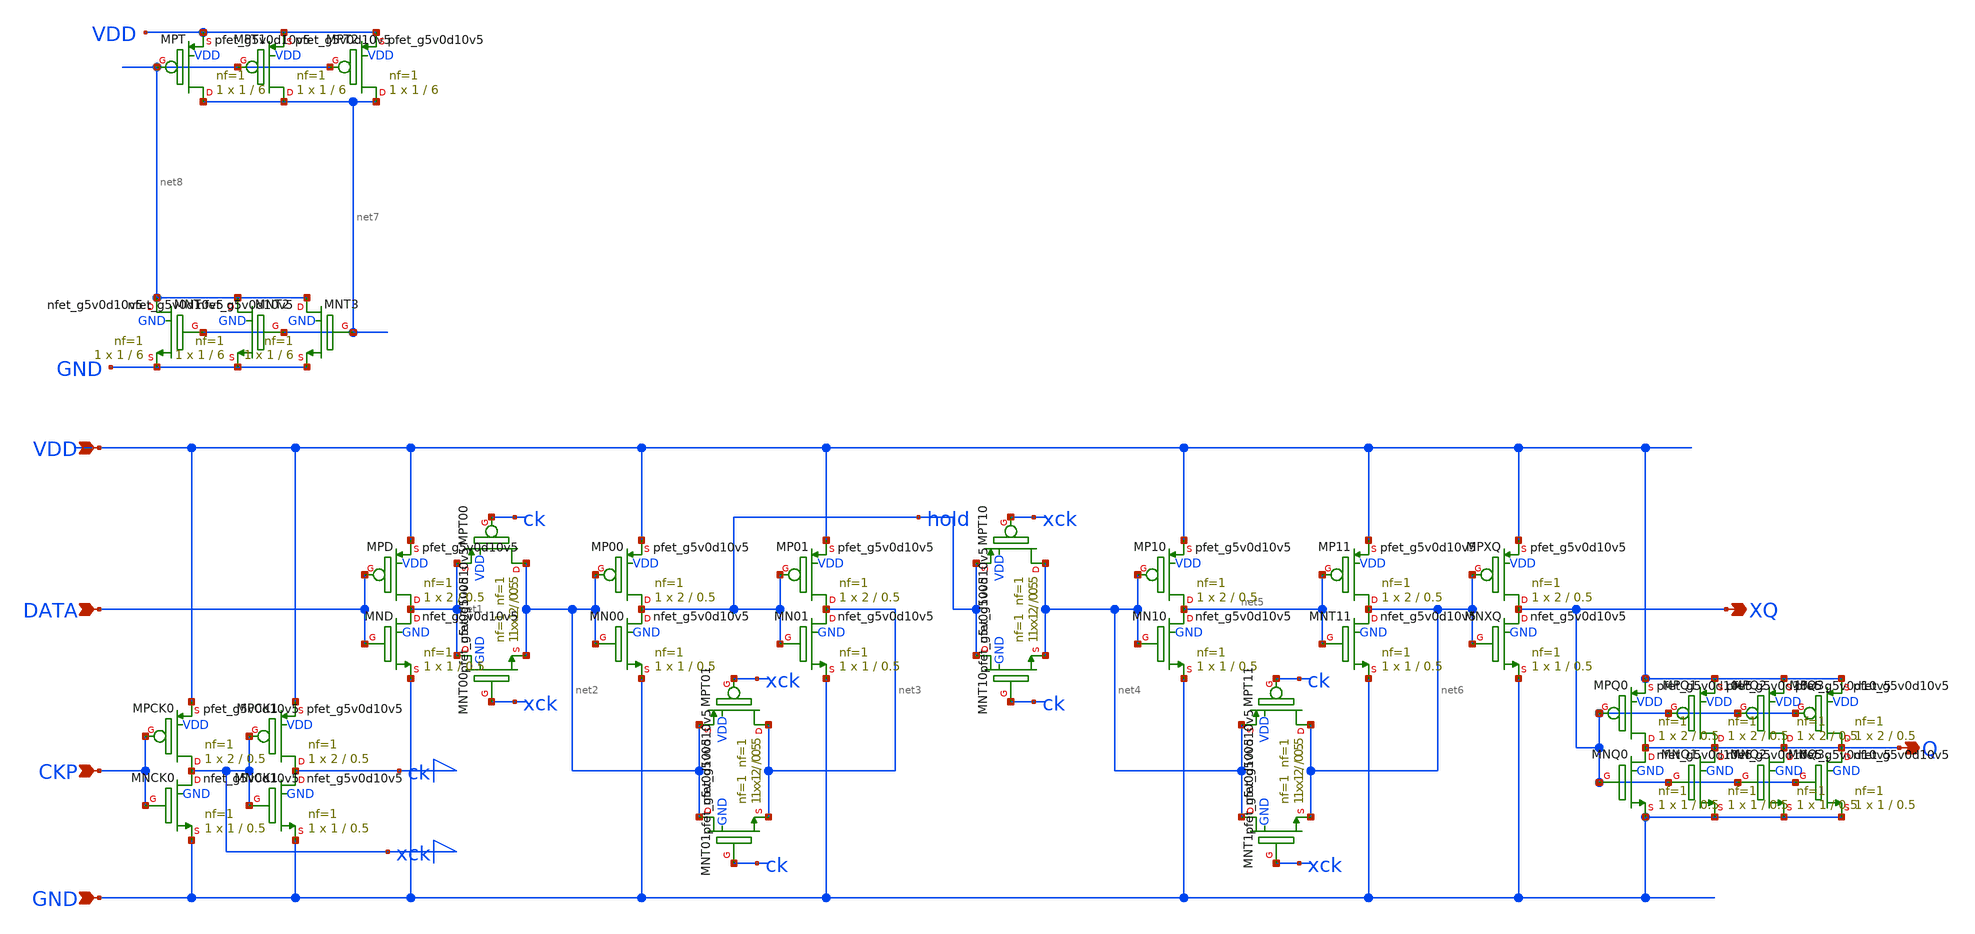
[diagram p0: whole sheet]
** sch_path: design/schematic/DFF3V3_v1.sch
**.subckt DFF3V3_v1 VDD DATA GND CKP XQ Q
*.ipin VDD
*.ipin DATA
*.ipin GND
*.ipin CKP
*.opin XQ
*.opin Q
XMNCK0 xck CKP GND GND sky130_fd_pr__nfet_g5v0d10v5 L=0.5 W=1 nf=1 ad='int((nf+1)/2) * W/nf * 0.29' as='int((nf+2)/2) * W/nf * 0.29'
+ pd='2*int((nf+1)/2) * (W/nf + 0.29)' ps='2*int((nf+2)/2) * (W/nf + 0.29)' nrd='0.29 / W' nrs='0.29 / W'
+ sa=0 sb=0 sd=0 mult=1 m=1
XMPCK0 xck CKP VDD VDD sky130_fd_pr__pfet_g5v0d10v5 L=0.5 W=2 nf=1 ad='int((nf+1)/2) * W/nf * 0.29' as='int((nf+2)/2) * W/nf * 0.29'
+ pd='2*int((nf+1)/2) * (W/nf + 0.29)' ps='2*int((nf+2)/2) * (W/nf + 0.29)' nrd='0.29 / W' nrs='0.29 / W'
+ sa=0 sb=0 sd=0 mult=1 m=1
XMNCK1 ck xck GND GND sky130_fd_pr__nfet_g5v0d10v5 L=0.5 W=1 nf=1 ad='int((nf+1)/2) * W/nf * 0.29' as='int((nf+2)/2) * W/nf * 0.29'
+ pd='2*int((nf+1)/2) * (W/nf + 0.29)' ps='2*int((nf+2)/2) * (W/nf + 0.29)' nrd='0.29 / W' nrs='0.29 / W'
+ sa=0 sb=0 sd=0 mult=1 m=1
XMPCK1 ck xck VDD VDD sky130_fd_pr__pfet_g5v0d10v5 L=0.5 W=2 nf=1 ad='int((nf+1)/2) * W/nf * 0.29' as='int((nf+2)/2) * W/nf * 0.29'
+ pd='2*int((nf+1)/2) * (W/nf + 0.29)' ps='2*int((nf+2)/2) * (W/nf + 0.29)' nrd='0.29 / W' nrs='0.29 / W'
+ sa=0 sb=0 sd=0 mult=1 m=1
XMPT00 net2 ck net1 VDD sky130_fd_pr__pfet_g5v0d10v5 L=0.5 W=2 nf=1 ad='int((nf+1)/2) * W/nf * 0.29'
+ as='int((nf+2)/2) * W/nf * 0.29' pd='2*int((nf+1)/2) * (W/nf + 0.29)' ps='2*int((nf+2)/2) * (W/nf + 0.29)'
+ nrd='0.29 / W' nrs='0.29 / W' sa=0 sb=0 sd=0 mult=1 m=1
XMNT00 net1 xck net2 GND sky130_fd_pr__nfet_g5v0d10v5 L=0.5 W=1 nf=1 ad='int((nf+1)/2) * W/nf * 0.29'
+ as='int((nf+2)/2) * W/nf * 0.29' pd='2*int((nf+1)/2) * (W/nf + 0.29)' ps='2*int((nf+2)/2) * (W/nf + 0.29)'
+ nrd='0.29 / W' nrs='0.29 / W' sa=0 sb=0 sd=0 mult=1 m=1
XMN00 hold net2 GND GND sky130_fd_pr__nfet_g5v0d10v5 L=0.5 W=1 nf=1 ad='int((nf+1)/2) * W/nf * 0.29'
+ as='int((nf+2)/2) * W/nf * 0.29' pd='2*int((nf+1)/2) * (W/nf + 0.29)' ps='2*int((nf+2)/2) * (W/nf + 0.29)'
+ nrd='0.29 / W' nrs='0.29 / W' sa=0 sb=0 sd=0 mult=1 m=1
XMP00 hold net2 VDD VDD sky130_fd_pr__pfet_g5v0d10v5 L=0.5 W=2 nf=1 ad='int((nf+1)/2) * W/nf * 0.29'
+ as='int((nf+2)/2) * W/nf * 0.29' pd='2*int((nf+1)/2) * (W/nf + 0.29)' ps='2*int((nf+2)/2) * (W/nf + 0.29)'
+ nrd='0.29 / W' nrs='0.29 / W' sa=0 sb=0 sd=0 mult=1 m=1
XMN01 net3 hold GND GND sky130_fd_pr__nfet_g5v0d10v5 L=0.5 W=1 nf=1 ad='int((nf+1)/2) * W/nf * 0.29'
+ as='int((nf+2)/2) * W/nf * 0.29' pd='2*int((nf+1)/2) * (W/nf + 0.29)' ps='2*int((nf+2)/2) * (W/nf + 0.29)'
+ nrd='0.29 / W' nrs='0.29 / W' sa=0 sb=0 sd=0 mult=1 m=1
XMP01 net3 hold VDD VDD sky130_fd_pr__pfet_g5v0d10v5 L=0.5 W=2 nf=1 ad='int((nf+1)/2) * W/nf * 0.29'
+ as='int((nf+2)/2) * W/nf * 0.29' pd='2*int((nf+1)/2) * (W/nf + 0.29)' ps='2*int((nf+2)/2) * (W/nf + 0.29)'
+ nrd='0.29 / W' nrs='0.29 / W' sa=0 sb=0 sd=0 mult=1 m=1
XMPT01 net3 xck net2 VDD sky130_fd_pr__pfet_g5v0d10v5 L=0.5 W=2 nf=1 ad='int((nf+1)/2) * W/nf * 0.29'
+ as='int((nf+2)/2) * W/nf * 0.29' pd='2*int((nf+1)/2) * (W/nf + 0.29)' ps='2*int((nf+2)/2) * (W/nf + 0.29)'
+ nrd='0.29 / W' nrs='0.29 / W' sa=0 sb=0 sd=0 mult=1 m=1
XMNT01 net2 ck net3 GND sky130_fd_pr__nfet_g5v0d10v5 L=0.5 W=1 nf=1 ad='int((nf+1)/2) * W/nf * 0.29'
+ as='int((nf+2)/2) * W/nf * 0.29' pd='2*int((nf+1)/2) * (W/nf + 0.29)' ps='2*int((nf+2)/2) * (W/nf + 0.29)'
+ nrd='0.29 / W' nrs='0.29 / W' sa=0 sb=0 sd=0 mult=1 m=1
XMPT10 net4 xck hold VDD sky130_fd_pr__pfet_g5v0d10v5 L=0.5 W=2 nf=1 ad='int((nf+1)/2) * W/nf * 0.29'
+ as='int((nf+2)/2) * W/nf * 0.29' pd='2*int((nf+1)/2) * (W/nf + 0.29)' ps='2*int((nf+2)/2) * (W/nf + 0.29)'
+ nrd='0.29 / W' nrs='0.29 / W' sa=0 sb=0 sd=0 mult=1 m=1
XMNT10 hold ck net4 GND sky130_fd_pr__nfet_g5v0d10v5 L=0.5 W=1 nf=1 ad='int((nf+1)/2) * W/nf * 0.29'
+ as='int((nf+2)/2) * W/nf * 0.29' pd='2*int((nf+1)/2) * (W/nf + 0.29)' ps='2*int((nf+2)/2) * (W/nf + 0.29)'
+ nrd='0.29 / W' nrs='0.29 / W' sa=0 sb=0 sd=0 mult=1 m=1
XMN10 net5 net4 GND GND sky130_fd_pr__nfet_g5v0d10v5 L=0.5 W=1 nf=1 ad='int((nf+1)/2) * W/nf * 0.29'
+ as='int((nf+2)/2) * W/nf * 0.29' pd='2*int((nf+1)/2) * (W/nf + 0.29)' ps='2*int((nf+2)/2) * (W/nf + 0.29)'
+ nrd='0.29 / W' nrs='0.29 / W' sa=0 sb=0 sd=0 mult=1 m=1
XMP10 net5 net4 VDD VDD sky130_fd_pr__pfet_g5v0d10v5 L=0.5 W=2 nf=1 ad='int((nf+1)/2) * W/nf * 0.29'
+ as='int((nf+2)/2) * W/nf * 0.29' pd='2*int((nf+1)/2) * (W/nf + 0.29)' ps='2*int((nf+2)/2) * (W/nf + 0.29)'
+ nrd='0.29 / W' nrs='0.29 / W' sa=0 sb=0 sd=0 mult=1 m=1
XMNT11 net6 net5 GND GND sky130_fd_pr__nfet_g5v0d10v5 L=0.5 W=1 nf=1 ad='int((nf+1)/2) * W/nf * 0.29'
+ as='int((nf+2)/2) * W/nf * 0.29' pd='2*int((nf+1)/2) * (W/nf + 0.29)' ps='2*int((nf+2)/2) * (W/nf + 0.29)'
+ nrd='0.29 / W' nrs='0.29 / W' sa=0 sb=0 sd=0 mult=1 m=1
XMP11 net6 net5 VDD VDD sky130_fd_pr__pfet_g5v0d10v5 L=0.5 W=2 nf=1 ad='int((nf+1)/2) * W/nf * 0.29'
+ as='int((nf+2)/2) * W/nf * 0.29' pd='2*int((nf+1)/2) * (W/nf + 0.29)' ps='2*int((nf+2)/2) * (W/nf + 0.29)'
+ nrd='0.29 / W' nrs='0.29 / W' sa=0 sb=0 sd=0 mult=1 m=1
XMPT11 net6 ck net4 VDD sky130_fd_pr__pfet_g5v0d10v5 L=0.5 W=2 nf=1 ad='int((nf+1)/2) * W/nf * 0.29'
+ as='int((nf+2)/2) * W/nf * 0.29' pd='2*int((nf+1)/2) * (W/nf + 0.29)' ps='2*int((nf+2)/2) * (W/nf + 0.29)'
+ nrd='0.29 / W' nrs='0.29 / W' sa=0 sb=0 sd=0 mult=1 m=1
XMNT1 net4 xck net6 GND sky130_fd_pr__nfet_g5v0d10v5 L=0.5 W=1 nf=1 ad='int((nf+1)/2) * W/nf * 0.29'
+ as='int((nf+2)/2) * W/nf * 0.29' pd='2*int((nf+1)/2) * (W/nf + 0.29)' ps='2*int((nf+2)/2) * (W/nf + 0.29)'
+ nrd='0.29 / W' nrs='0.29 / W' sa=0 sb=0 sd=0 mult=1 m=1
XMNXQ XQ net6 GND GND sky130_fd_pr__nfet_g5v0d10v5 L=0.5 W=1 nf=1 ad='int((nf+1)/2) * W/nf * 0.29' as='int((nf+2)/2) * W/nf * 0.29'
+ pd='2*int((nf+1)/2) * (W/nf + 0.29)' ps='2*int((nf+2)/2) * (W/nf + 0.29)' nrd='0.29 / W' nrs='0.29 / W'
+ sa=0 sb=0 sd=0 mult=1 m=1
XMPXQ XQ net6 VDD VDD sky130_fd_pr__pfet_g5v0d10v5 L=0.5 W=2 nf=1 ad='int((nf+1)/2) * W/nf * 0.29' as='int((nf+2)/2) * W/nf * 0.29'
+ pd='2*int((nf+1)/2) * (W/nf + 0.29)' ps='2*int((nf+2)/2) * (W/nf + 0.29)' nrd='0.29 / W' nrs='0.29 / W'
+ sa=0 sb=0 sd=0 mult=1 m=1
XMNQ0 Q XQ GND GND sky130_fd_pr__nfet_g5v0d10v5 L=0.5 W=1 nf=1 ad='int((nf+1)/2) * W/nf * 0.29' as='int((nf+2)/2) * W/nf * 0.29'
+ pd='2*int((nf+1)/2) * (W/nf + 0.29)' ps='2*int((nf+2)/2) * (W/nf + 0.29)' nrd='0.29 / W' nrs='0.29 / W'
+ sa=0 sb=0 sd=0 mult=1 m=1
XMPQ0 Q XQ VDD VDD sky130_fd_pr__pfet_g5v0d10v5 L=0.5 W=2 nf=1 ad='int((nf+1)/2) * W/nf * 0.29' as='int((nf+2)/2) * W/nf * 0.29'
+ pd='2*int((nf+1)/2) * (W/nf + 0.29)' ps='2*int((nf+2)/2) * (W/nf + 0.29)' nrd='0.29 / W' nrs='0.29 / W'
+ sa=0 sb=0 sd=0 mult=1 m=1
XMND net1 DATA GND GND sky130_fd_pr__nfet_g5v0d10v5 L=0.5 W=1 nf=1 ad='int((nf+1)/2) * W/nf * 0.29' as='int((nf+2)/2) * W/nf * 0.29'
+ pd='2*int((nf+1)/2) * (W/nf + 0.29)' ps='2*int((nf+2)/2) * (W/nf + 0.29)' nrd='0.29 / W' nrs='0.29 / W'
+ sa=0 sb=0 sd=0 mult=1 m=1
XMPD net1 DATA VDD VDD sky130_fd_pr__pfet_g5v0d10v5 L=0.5 W=2 nf=1 ad='int((nf+1)/2) * W/nf * 0.29' as='int((nf+2)/2) * W/nf * 0.29'
+ pd='2*int((nf+1)/2) * (W/nf + 0.29)' ps='2*int((nf+2)/2) * (W/nf + 0.29)' nrd='0.29 / W' nrs='0.29 / W'
+ sa=0 sb=0 sd=0 mult=1 m=1
XMNQ1 Q XQ GND GND sky130_fd_pr__nfet_g5v0d10v5 L=0.5 W=1 nf=1 ad='int((nf+1)/2) * W/nf * 0.29' as='int((nf+2)/2) * W/nf * 0.29'
+ pd='2*int((nf+1)/2) * (W/nf + 0.29)' ps='2*int((nf+2)/2) * (W/nf + 0.29)' nrd='0.29 / W' nrs='0.29 / W'
+ sa=0 sb=0 sd=0 mult=1 m=1
XMNQ2 Q XQ GND GND sky130_fd_pr__nfet_g5v0d10v5 L=0.5 W=1 nf=1 ad='int((nf+1)/2) * W/nf * 0.29' as='int((nf+2)/2) * W/nf * 0.29'
+ pd='2*int((nf+1)/2) * (W/nf + 0.29)' ps='2*int((nf+2)/2) * (W/nf + 0.29)' nrd='0.29 / W' nrs='0.29 / W'
+ sa=0 sb=0 sd=0 mult=1 m=1
XMPQ1 Q XQ VDD VDD sky130_fd_pr__pfet_g5v0d10v5 L=0.5 W=2 nf=1 ad='int((nf+1)/2) * W/nf * 0.29' as='int((nf+2)/2) * W/nf * 0.29'
+ pd='2*int((nf+1)/2) * (W/nf + 0.29)' ps='2*int((nf+2)/2) * (W/nf + 0.29)' nrd='0.29 / W' nrs='0.29 / W'
+ sa=0 sb=0 sd=0 mult=1 m=1
XMPQ2 Q XQ VDD VDD sky130_fd_pr__pfet_g5v0d10v5 L=0.5 W=2 nf=1 ad='int((nf+1)/2) * W/nf * 0.29' as='int((nf+2)/2) * W/nf * 0.29'
+ pd='2*int((nf+1)/2) * (W/nf + 0.29)' ps='2*int((nf+2)/2) * (W/nf + 0.29)' nrd='0.29 / W' nrs='0.29 / W'
+ sa=0 sb=0 sd=0 mult=1 m=1
XMPQ3 Q XQ VDD VDD sky130_fd_pr__pfet_g5v0d10v5 L=0.5 W=2 nf=1 ad='int((nf+1)/2) * W/nf * 0.29' as='int((nf+2)/2) * W/nf * 0.29'
+ pd='2*int((nf+1)/2) * (W/nf + 0.29)' ps='2*int((nf+2)/2) * (W/nf + 0.29)' nrd='0.29 / W' nrs='0.29 / W'
+ sa=0 sb=0 sd=0 mult=1 m=1
XMNQ3 Q XQ GND GND sky130_fd_pr__nfet_g5v0d10v5 L=0.5 W=1 nf=1 ad='int((nf+1)/2) * W/nf * 0.29' as='int((nf+2)/2) * W/nf * 0.29'
+ pd='2*int((nf+1)/2) * (W/nf + 0.29)' ps='2*int((nf+2)/2) * (W/nf + 0.29)' nrd='0.29 / W' nrs='0.29 / W'
+ sa=0 sb=0 sd=0 mult=1 m=1
XMPT net7 net8 VDD VDD sky130_fd_pr__pfet_g5v0d10v5 L=6 W=1 nf=1 ad='int((nf+1)/2) * W/nf * 0.29' as='int((nf+2)/2) * W/nf * 0.29'
+ pd='2*int((nf+1)/2) * (W/nf + 0.29)' ps='2*int((nf+2)/2) * (W/nf + 0.29)' nrd='0.29 / W' nrs='0.29 / W'
+ sa=0 sb=0 sd=0 mult=1 m=1
XMNT net8 net7 GND GND sky130_fd_pr__nfet_g5v0d10v5 L=6 W=1 nf=1 ad='int((nf+1)/2) * W/nf * 0.29' as='int((nf+2)/2) * W/nf * 0.29'
+ pd='2*int((nf+1)/2) * (W/nf + 0.29)' ps='2*int((nf+2)/2) * (W/nf + 0.29)' nrd='0.29 / W' nrs='0.29 / W'
+ sa=0 sb=0 sd=0 mult=1 m=1
XMPT1 net7 net8 VDD VDD sky130_fd_pr__pfet_g5v0d10v5 L=6 W=1 nf=1 ad='int((nf+1)/2) * W/nf * 0.29' as='int((nf+2)/2) * W/nf * 0.29'
+ pd='2*int((nf+1)/2) * (W/nf + 0.29)' ps='2*int((nf+2)/2) * (W/nf + 0.29)' nrd='0.29 / W' nrs='0.29 / W'
+ sa=0 sb=0 sd=0 mult=1 m=1
XMPT2 net7 net8 VDD VDD sky130_fd_pr__pfet_g5v0d10v5 L=6 W=1 nf=1 ad='int((nf+1)/2) * W/nf * 0.29' as='int((nf+2)/2) * W/nf * 0.29'
+ pd='2*int((nf+1)/2) * (W/nf + 0.29)' ps='2*int((nf+2)/2) * (W/nf + 0.29)' nrd='0.29 / W' nrs='0.29 / W'
+ sa=0 sb=0 sd=0 mult=1 m=1
XMNT2 net8 net7 GND GND sky130_fd_pr__nfet_g5v0d10v5 L=6 W=1 nf=1 ad='int((nf+1)/2) * W/nf * 0.29' as='int((nf+2)/2) * W/nf * 0.29'
+ pd='2*int((nf+1)/2) * (W/nf + 0.29)' ps='2*int((nf+2)/2) * (W/nf + 0.29)' nrd='0.29 / W' nrs='0.29 / W'
+ sa=0 sb=0 sd=0 mult=1 m=1
XMNT3 net8 net7 GND GND sky130_fd_pr__nfet_g5v0d10v5 L=6 W=1 nf=1 ad='int((nf+1)/2) * W/nf * 0.29' as='int((nf+2)/2) * W/nf * 0.29'
+ pd='2*int((nf+1)/2) * (W/nf + 0.29)' ps='2*int((nf+2)/2) * (W/nf + 0.29)' nrd='0.29 / W' nrs='0.29 / W'
+ sa=0 sb=0 sd=0 mult=1 m=1
**.ends
.end
